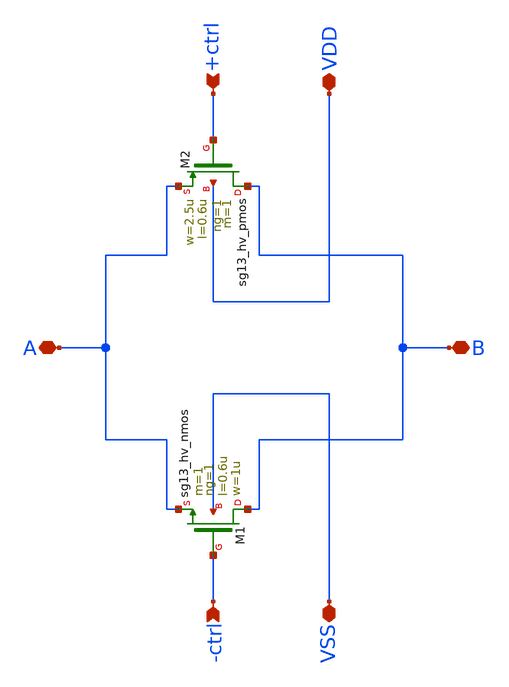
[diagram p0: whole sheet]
** sch_path: real_circuit/final/TG.sch
**.subckt TG A B VDD VSS +ctrl -ctrl
*.iopin A
*.iopin B
*.iopin VDD
*.iopin VSS
*.ipin +ctrl
*.ipin -ctrl
XM1 B -ctrl A VSS sg13_hv_nmos w=1u l=0.6u ng=1 m=1 mm_ok=1
XM2 B +ctrl A VDD sg13_hv_pmos w=2.5u l=0.6u ng=1 m=1 mm_ok=1
**.ends
.end
